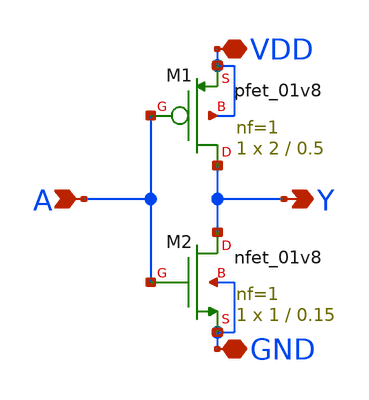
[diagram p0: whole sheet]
** sch_path: inverter/xschem/inverter.sch
**.subckt inverter GND VDD Y A
*.iopin GND
*.iopin VDD
*.opin Y
*.ipin A
XM1 Y A VDD VDD sky130_fd_pr__pfet_01v8 L=0.5 W=2 nf=1 ad='int((nf+1)/2) * W/nf * 0.29' as='int((nf+2)/2) * W/nf * 0.29'
+ pd='2*int((nf+1)/2) * (W/nf + 0.29)' ps='2*int((nf+2)/2) * (W/nf + 0.29)' nrd='0.29 / W' nrs='0.29 / W'
+ sa=0 sb=0 sd=0 mult=1 m=1
XM2 Y A GND GND sky130_fd_pr__nfet_01v8 L=0.15 W=1 nf=1 ad='int((nf+1)/2) * W/nf * 0.29' as='int((nf+2)/2) * W/nf * 0.29'
+ pd='2*int((nf+1)/2) * (W/nf + 0.29)' ps='2*int((nf+2)/2) * (W/nf + 0.29)' nrd='0.29 / W' nrs='0.29 / W'
+ sa=0 sb=0 sd=0 mult=1 m=1
**.ends
.end
